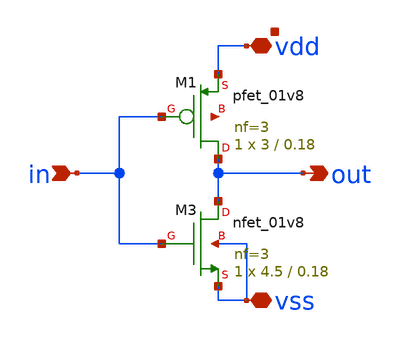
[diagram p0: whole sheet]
** sch_path: inverter/xschem/inverter_updated.sch
**.subckt inverter_updated in vss vdd out
*.ipin in
*.iopin vss
*.iopin vdd
*.opin out
XM1 out in vdd net1 sky130_fd_pr__pfet_01v8 L=0.18 W=3 nf=3 ad='int((3 + 1)/2) * 3 / 3 * 0.29' as='int((3 + 2)/2) * 3 / 3 * 0.29'
+ pd='2*int((3 + 1)/2) * (3 / 3 + 0.29)' ps='2*int((3 + 2)/2) * (3 / 3 + 0.29)' nrd='0.29 / 3 ' nrs='0.29 / 3 '
+ sa=0 sb=0 sd=0 mult=1 m=1
XM3 out in vss vss sky130_fd_pr__nfet_01v8 L=0.18 W=4.5 nf=3 ad='int((3 + 1)/2) * 4.5 / 3 * 0.29' as='int((3 + 2)/2) * 4.5 / 3 * 0.29'
+ pd='2*int((3 + 1)/2) * (4.5 / 3 + 0.29)' ps='2*int((3 + 2)/2) * (4.5 / 3 + 0.29)' nrd='0.29 / 4.5 ' nrs='0.29 / 4.5 '
+ sa=0 sb=0 sd=0 mult=1 m=1
**.ends
.end
